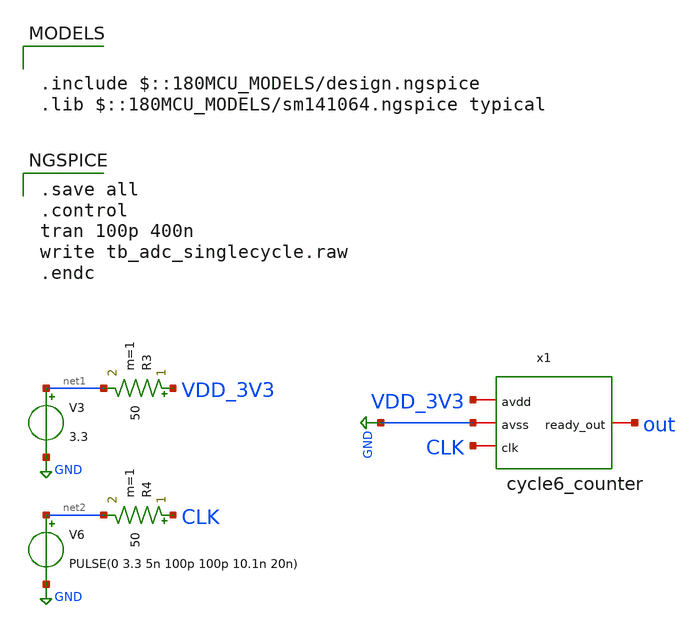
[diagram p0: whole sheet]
** sch_path: designs/libs/adc_singlecycle/tb_adc_singlecycle.sch
**.subckt tb_adc_singlecycle
V3 net1 GND 3.3
V6 net2 GND PULSE(0 3.3 5n 100p 100p 10.1n 20n)
R3 VDD_3V3 net1 50 m=1
R4 CLK net2 50 m=1
x1 out VDD_3V3 GND CLK cycle6_counter
**** begin user architecture code

.include $::180MCU_MODELS/design.ngspice
.lib $::180MCU_MODELS/sm141064.ngspice typical


.save all
.control
tran 100p 400n
write tb_adc_singlecycle.raw
.endc

**** end user architecture code
**.ends
.GLOBAL GND
.end
